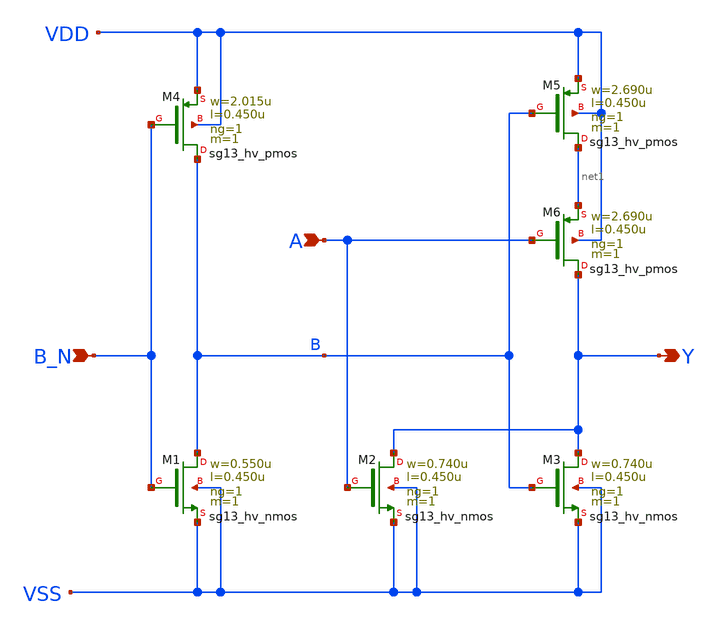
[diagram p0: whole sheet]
** sch_path: ihp-sg13g2/libs.ref/sg13g2_stdcell_hv/sch/xschem/sg13g2_hv_nor2b_1.sch
* Copyright 2023 IHP PDK Authors
* Licensed under the Apache License, Version 2.0 (the "License");
* you may not use this file except in compliance with the License.
* You may obtain a copy of the License at
* https://www.apache.org/licenses/LICENSE-2.0
* Unless required by applicable law or agreed to in writing, software
* distributed under the License is distributed on an "AS IS" BASIS,
* WITHOUT WARRANTIES OR CONDITIONS OF ANY KIND, either express or implied.
* See the License for the specific language governing permissions and
* limitations under the License.
**.subckt sg13g2_hv_nor2b_1 Y B_N A
*.opin Y
*.ipin B_N
*.ipin A
XM1 B B_N VSS VSS sg13_hv_nmos w=0.550u l=0.450u ng=1 m=1 mm_ok=1
XM2 Y A VSS VSS sg13_hv_nmos w=0.740u l=0.450u ng=1 m=1 mm_ok=1
XM3 Y B VSS VSS sg13_hv_nmos w=0.740u l=0.450u ng=1 m=1 mm_ok=1
XM4 B B_N VDD VDD sg13_hv_pmos w=2.015u l=0.450u ng=1 m=1 mm_ok=1
XM5 net1 B VDD VDD sg13_hv_pmos w=2.690u l=0.450u ng=1 m=1 mm_ok=1
XM6 Y A net1 VDD sg13_hv_pmos w=2.690u l=0.450u ng=1 m=1 mm_ok=1
**.ends
.end
